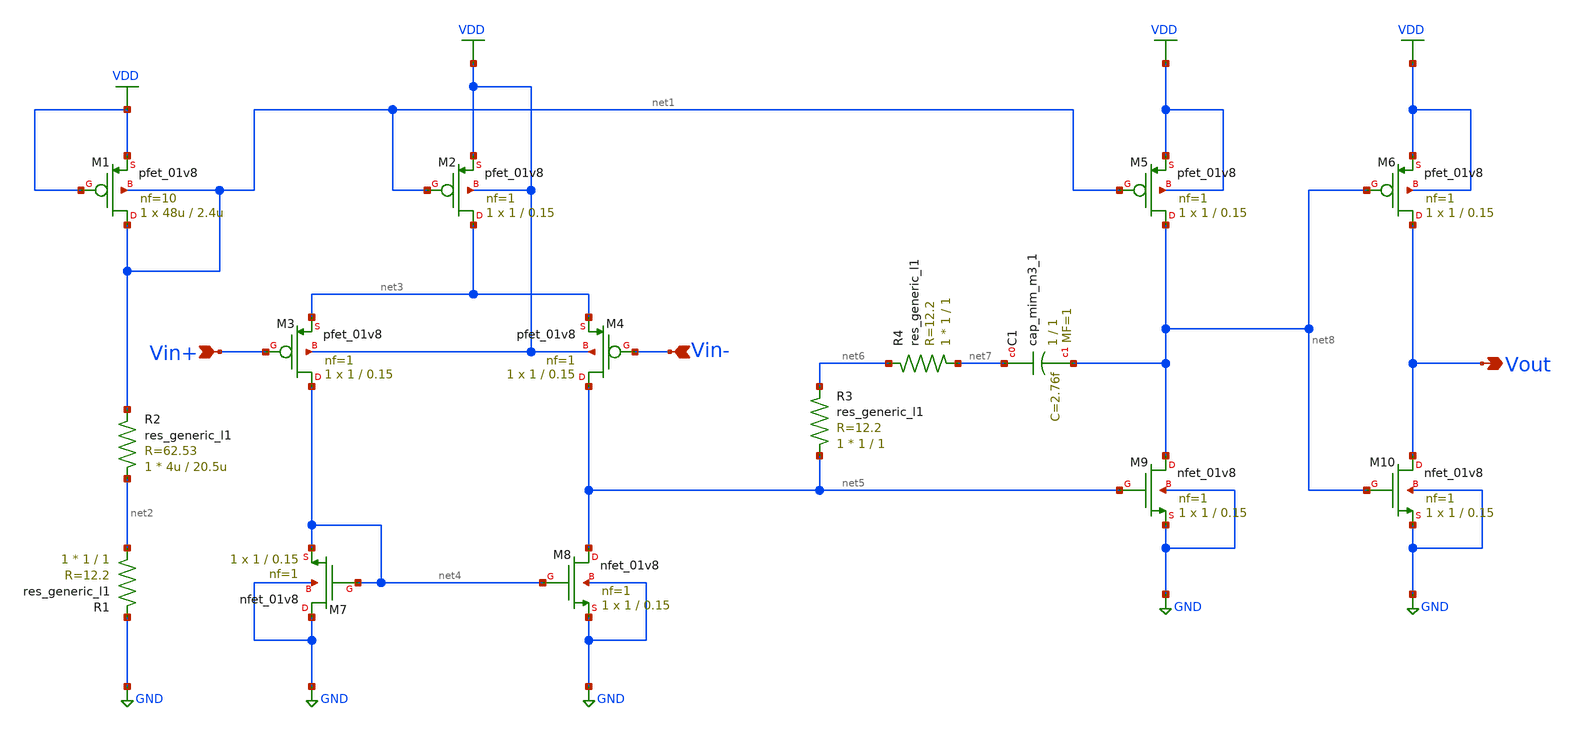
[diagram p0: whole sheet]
** sch_path: op-amp/op-amp_ver_test.sch
**.subckt op-amp_ver_test Vin+ Vin- Vout
*.ipin Vin+
*.ipin Vin-
*.opin Vout
XM1 net1 VDD VDD net1 sky130_fd_pr__pfet_01v8 L=2.4u W=48u nf=10 ad='int((nf+1)/2) * W/nf * 0.29' as='int((nf+2)/2) * W/nf * 0.29'
+ pd='2*int((nf+1)/2) * (W/nf + 0.29)' ps='2*int((nf+2)/2) * (W/nf + 0.29)' nrd='0.29 / W' nrs='0.29 / W'
+ sa=0 sb=0 sd=0 mult=1 m=1
XM2 net3 net1 VDD VDD sky130_fd_pr__pfet_01v8 L=0.15 W=1 nf=1 ad='int((nf+1)/2) * W/nf * 0.29' as='int((nf+2)/2) * W/nf * 0.29'
+ pd='2*int((nf+1)/2) * (W/nf + 0.29)' ps='2*int((nf+2)/2) * (W/nf + 0.29)' nrd='0.29 / W' nrs='0.29 / W'
+ sa=0 sb=0 sd=0 mult=1 m=1
XM3 net4 Vin+ net3 VDD sky130_fd_pr__pfet_01v8 L=0.15 W=1 nf=1 ad='int((nf+1)/2) * W/nf * 0.29' as='int((nf+2)/2) * W/nf * 0.29'
+ pd='2*int((nf+1)/2) * (W/nf + 0.29)' ps='2*int((nf+2)/2) * (W/nf + 0.29)' nrd='0.29 / W' nrs='0.29 / W'
+ sa=0 sb=0 sd=0 mult=1 m=1
XM4 net5 Vin- net3 VDD sky130_fd_pr__pfet_01v8 L=0.15 W=1 nf=1 ad='int((nf+1)/2) * W/nf * 0.29' as='int((nf+2)/2) * W/nf * 0.29'
+ pd='2*int((nf+1)/2) * (W/nf + 0.29)' ps='2*int((nf+2)/2) * (W/nf + 0.29)' nrd='0.29 / W' nrs='0.29 / W'
+ sa=0 sb=0 sd=0 mult=1 m=1
XM5 net8 net1 VDD VDD sky130_fd_pr__pfet_01v8 L=0.15 W=1 nf=1 ad='int((nf+1)/2) * W/nf * 0.29' as='int((nf+2)/2) * W/nf * 0.29'
+ pd='2*int((nf+1)/2) * (W/nf + 0.29)' ps='2*int((nf+2)/2) * (W/nf + 0.29)' nrd='0.29 / W' nrs='0.29 / W'
+ sa=0 sb=0 sd=0 mult=1 m=1
XM6 Vout net8 VDD VDD sky130_fd_pr__pfet_01v8 L=0.15 W=1 nf=1 ad='int((nf+1)/2) * W/nf * 0.29' as='int((nf+2)/2) * W/nf * 0.29'
+ pd='2*int((nf+1)/2) * (W/nf + 0.29)' ps='2*int((nf+2)/2) * (W/nf + 0.29)' nrd='0.29 / W' nrs='0.29 / W'
+ sa=0 sb=0 sd=0 mult=1 m=1
XM7 GND net4 net4 GND sky130_fd_pr__nfet_01v8 L=0.15 W=1 nf=1 ad='int((nf+1)/2) * W/nf * 0.29' as='int((nf+2)/2) * W/nf * 0.29'
+ pd='2*int((nf+1)/2) * (W/nf + 0.29)' ps='2*int((nf+2)/2) * (W/nf + 0.29)' nrd='0.29 / W' nrs='0.29 / W'
+ sa=0 sb=0 sd=0 mult=1 m=1
XM8 net5 net4 GND GND sky130_fd_pr__nfet_01v8 L=0.15 W=1 nf=1 ad='int((nf+1)/2) * W/nf * 0.29' as='int((nf+2)/2) * W/nf * 0.29'
+ pd='2*int((nf+1)/2) * (W/nf + 0.29)' ps='2*int((nf+2)/2) * (W/nf + 0.29)' nrd='0.29 / W' nrs='0.29 / W'
+ sa=0 sb=0 sd=0 mult=1 m=1
XM9 net8 net5 GND GND sky130_fd_pr__nfet_01v8 L=0.15 W=1 nf=1 ad='int((nf+1)/2) * W/nf * 0.29' as='int((nf+2)/2) * W/nf * 0.29'
+ pd='2*int((nf+1)/2) * (W/nf + 0.29)' ps='2*int((nf+2)/2) * (W/nf + 0.29)' nrd='0.29 / W' nrs='0.29 / W'
+ sa=0 sb=0 sd=0 mult=1 m=1
XM10 Vout net8 GND GND sky130_fd_pr__nfet_01v8 L=0.15 W=1 nf=1 ad='int((nf+1)/2) * W/nf * 0.29' as='int((nf+2)/2) * W/nf * 0.29'
+ pd='2*int((nf+1)/2) * (W/nf + 0.29)' ps='2*int((nf+2)/2) * (W/nf + 0.29)' nrd='0.29 / W' nrs='0.29 / W'
+ sa=0 sb=0 sd=0 mult=1 m=1
R1 net2 GND sky130_fd_pr__res_generic_l1 W=1 L=1 m=1
R2 net2 net1 sky130_fd_pr__res_generic_l1 W=4u L=20.5u m=1
R3 net5 net6 sky130_fd_pr__res_generic_l1 W=1 L=1 m=1
R4 net7 net6 sky130_fd_pr__res_generic_l1 W=1 L=1 m=1
XC1 net7 net8 sky130_fd_pr__cap_mim_m3_1 W=1 L=1 MF=1 m=1
**.ends
.GLOBAL VDD
.GLOBAL GND
.end
